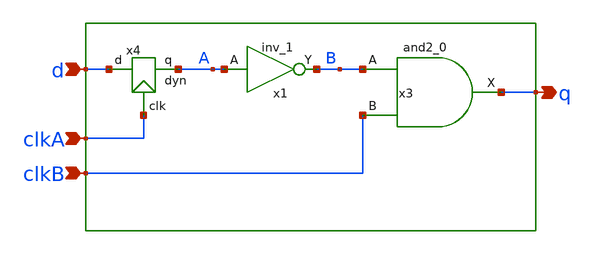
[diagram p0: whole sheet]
** sch_path: src/xe/test_cases/dyn_and.sch
**.subckt dyn_and d clkA q clkB
*.ipin d
*.ipin clkA
*.opin q
*.ipin clkB
x1 A vss vss vcc vcc B sky130_fd_sc_hd__inv_1
x3 B clkB vss vss vcc vcc q sky130_fd_sc_hd__and2_0
x4 clkA A d dyn
**.ends

* expanding   symbol:  yxt/dyn.sym # of pins=3
** sym_path: src/xe/test_cases/dyn.sym
** sch_path: src/xe/test_cases/dyn.sch
.subckt dyn clk q d
*.ipin clk
*.opin q
*.ipin d
x1 net1 vss vss vcc vcc q sky130_fd_sc_hd__inv_1
XM1 net1 d net2 vss sky130_fd_pr__nfet_01v8 L=0.15 W=1 nf=1 ad='int((nf+1)/2) * W/nf * 0.29' as='int((nf+2)/2) * W/nf * 0.29'
+ pd='2*int((nf+1)/2) * (W/nf + 0.29)' ps='2*int((nf+2)/2) * (W/nf + 0.29)' nrd='0.29 / W' nrs='0.29 / W'
+ sa=0 sb=0 sd=0 mult=1 m=1
XM2 net1 q vcc vcc sky130_fd_pr__pfet_01v8 L=0.15 W=1 nf=1 ad='int((nf+1)/2) * W/nf * 0.29' as='int((nf+2)/2) * W/nf * 0.29'
+ pd='2*int((nf+1)/2) * (W/nf + 0.29)' ps='2*int((nf+2)/2) * (W/nf + 0.29)' nrd='0.29 / W' nrs='0.29 / W'
+ sa=0 sb=0 sd=0 mult=1 m=1
XM3 net1 clk vcc vcc sky130_fd_pr__pfet_01v8 L=0.15 W=1 nf=1 ad='int((nf+1)/2) * W/nf * 0.29' as='int((nf+2)/2) * W/nf * 0.29'
+ pd='2*int((nf+1)/2) * (W/nf + 0.29)' ps='2*int((nf+2)/2) * (W/nf + 0.29)' nrd='0.29 / W' nrs='0.29 / W'
+ sa=0 sb=0 sd=0 mult=1 m=1
XM4 net2 clk vss vss sky130_fd_pr__nfet_01v8 L=0.15 W=1 nf=1 ad='int((nf+1)/2) * W/nf * 0.29' as='int((nf+2)/2) * W/nf * 0.29'
+ pd='2*int((nf+1)/2) * (W/nf + 0.29)' ps='2*int((nf+2)/2) * (W/nf + 0.29)' nrd='0.29 / W' nrs='0.29 / W'
+ sa=0 sb=0 sd=0 mult=1 m=1
.ends

.end
